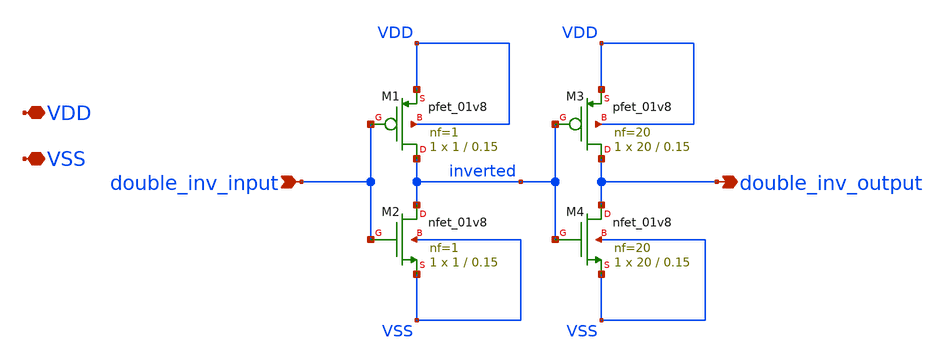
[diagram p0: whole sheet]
** sch_path: xschem/double_inverter.sch
**.subckt double_inverter VDD VSS double_inv_input double_inv_output
*.iopin VDD
*.iopin VSS
*.ipin double_inv_input
*.opin double_inv_output
XM1 inverted double_inv_input VDD VDD sky130_fd_pr__pfet_01v8 L=0.15 W=1 nf=1 ad='int((nf+1)/2) * W/nf * 0.29'
+ as='int((nf+2)/2) * W/nf * 0.29' pd='2*int((nf+1)/2) * (W/nf + 0.29)' ps='2*int((nf+2)/2) * (W/nf + 0.29)'
+ nrd='0.29 / W' nrs='0.29 / W' sa=0 sb=0 sd=0 mult=1 m=1
XM2 inverted double_inv_input VSS VSS sky130_fd_pr__nfet_01v8 L=0.15 W=1 nf=1 ad='int((nf+1)/2) * W/nf * 0.29'
+ as='int((nf+2)/2) * W/nf * 0.29' pd='2*int((nf+1)/2) * (W/nf + 0.29)' ps='2*int((nf+2)/2) * (W/nf + 0.29)'
+ nrd='0.29 / W' nrs='0.29 / W' sa=0 sb=0 sd=0 mult=1 m=1
XM3 double_inv_output inverted VDD VDD sky130_fd_pr__pfet_01v8 L=0.15 W=20 nf=20 ad='int((nf+1)/2) * W/nf * 0.29'
+ as='int((nf+2)/2) * W/nf * 0.29' pd='2*int((nf+1)/2) * (W/nf + 0.29)' ps='2*int((nf+2)/2) * (W/nf + 0.29)'
+ nrd='0.29 / W' nrs='0.29 / W' sa=0 sb=0 sd=0 mult=1 m=1
XM4 double_inv_output inverted VSS VSS sky130_fd_pr__nfet_01v8 L=0.15 W=20 nf=20 ad='int((nf+1)/2) * W/nf * 0.29'
+ as='int((nf+2)/2) * W/nf * 0.29' pd='2*int((nf+1)/2) * (W/nf + 0.29)' ps='2*int((nf+2)/2) * (W/nf + 0.29)'
+ nrd='0.29 / W' nrs='0.29 / W' sa=0 sb=0 sd=0 mult=1 m=1
**.ends
.end
